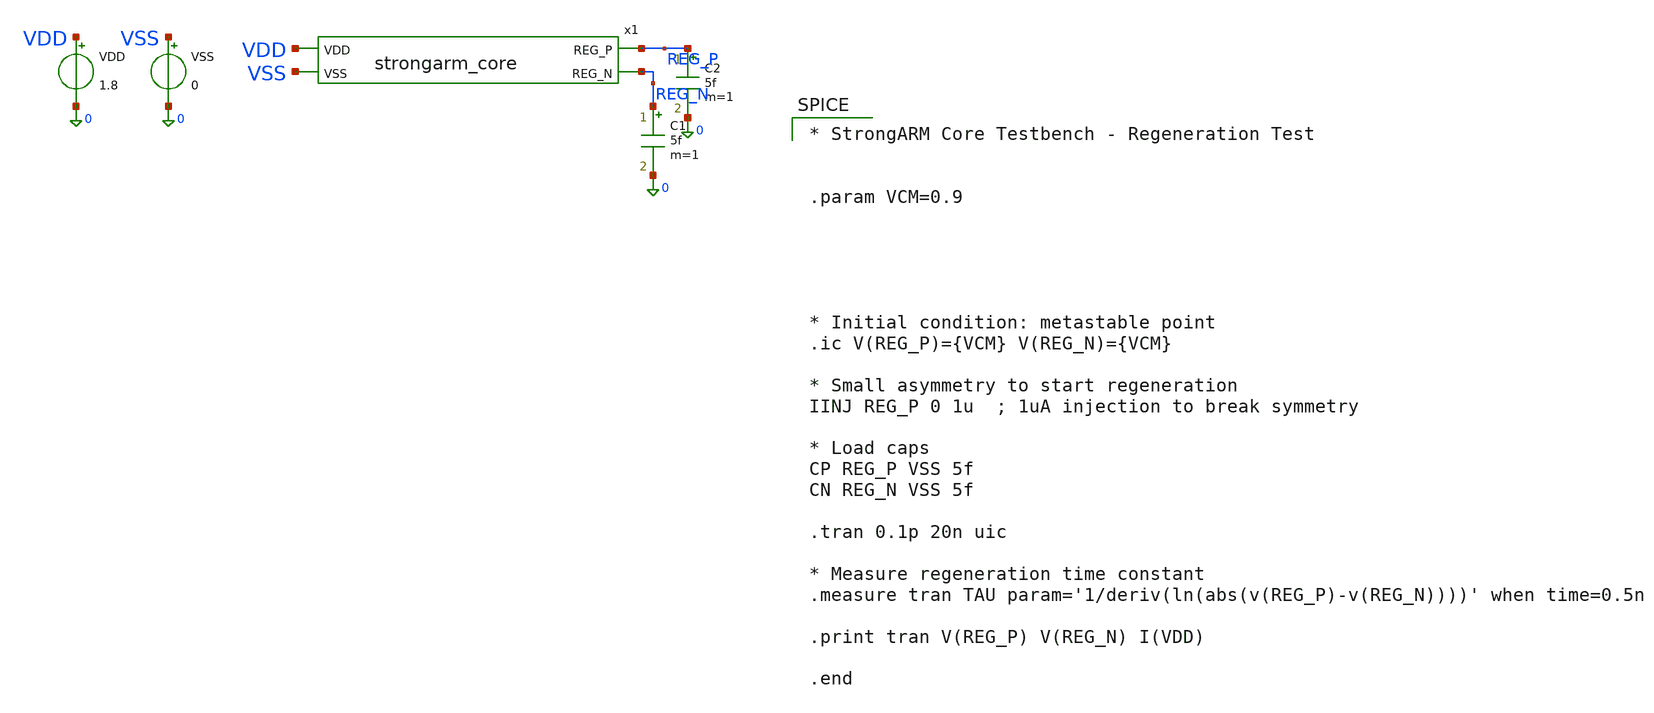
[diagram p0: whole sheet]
** sch_path: tb_strongarmcore.sch
**.subckt tb_strongarmcore
VSS VSS 0 0
VDD VDD 0 1.8
x1 VDD REG_P REG_N VSS strongarm_core
C1 REG_N 0 5f m=1
C2 REG_P 0 5f m=1
**** begin user architecture code

** opencircuitdesign pdks install
.lib $::SKYWATER_MODELS/sky130.lib.spice tt


* StrongARM Core Testbench - Regeneration Test


.param VCM=0.9





* Initial condition: metastable point
.ic V(REG_P)={VCM} V(REG_N)={VCM}

* Small asymmetry to start regeneration
IINJ REG_P 0 1u  ; 1uA injection to break symmetry

* Load caps
CP REG_P VSS 5f
CN REG_N VSS 5f

.tran 0.1p 20n uic

* Measure regeneration time constant
.measure tran TAU param='1/deriv(ln(abs(v(REG_P)-v(REG_N))))' when time=0.5n

.print tran V(REG_P) V(REG_N) I(VDD)

.end

**** end user architecture code
**.ends

* expanding   symbol:  /home/master/Documents/6_bit_Flash_ADC/strongarm_core.sym # of pins=4
** sym_path: strongarm_core.sym
** sch_path: strongarm_core.sch
.subckt strongarm_core VDD REG_P REG_N VSS
*.ipin VDD
*.ipin VSS
*.opin REG_P
*.opin REG_N
XM8 REG_P REG_N VDD VDD sky130_fd_pr__pfet_01v8 L=0.15 W=12 nf=1 ad='int((1 + 1)/2) * 12 / 1 * 0.29'
+ as='int((1 + 2)/2) * 12 / 1 * 0.29' pd='2*int((1 + 1)/2) * (12 / 1 + 0.29)' ps='2*int((1 + 2)/2) * (12 / 1 + 0.29)'
+ nrd='0.29 / 12 ' nrs='0.29 / 12 ' sa=0 sb=0 sd=0 mult=1 m=1
XM6 REG_P REG_N VSS VSS sky130_fd_pr__nfet_01v8 L=0.15 W=6 nf=1 ad='int((1 + 1)/2) * 6 / 1 * 0.29' as='int((1 + 2)/2) * 6 / 1 * 0.29'
+ pd='2*int((1 + 1)/2) * (6 / 1 + 0.29)' ps='2*int((1 + 2)/2) * (6 / 1 + 0.29)' nrd='0.29 / 6 ' nrs='0.29 / 6 '
+ sa=0 sb=0 sd=0 mult=1 m=1
XM5 REG_N REG_P VSS VSS sky130_fd_pr__nfet_01v8 L=0.15 W=6 nf=1 ad='int((1 + 1)/2) * 6 / 1 * 0.29' as='int((1 + 2)/2) * 6 / 1 * 0.29'
+ pd='2*int((1 + 1)/2) * (6 / 1 + 0.29)' ps='2*int((1 + 2)/2) * (6 / 1 + 0.29)' nrd='0.29 / 6 ' nrs='0.29 / 6 '
+ sa=0 sb=0 sd=0 mult=1 m=1
XM7 REG_N REG_P VDD VDD sky130_fd_pr__pfet_01v8 L=0.15 W=12 nf=1 ad='int((1 + 1)/2) * 12 / 1 * 0.29'
+ as='int((1 + 2)/2) * 12 / 1 * 0.29' pd='2*int((1 + 1)/2) * (12 / 1 + 0.29)' ps='2*int((1 + 2)/2) * (12 / 1 + 0.29)'
+ nrd='0.29 / 12 ' nrs='0.29 / 12 ' sa=0 sb=0 sd=0 mult=1 m=1
.ends

.end
